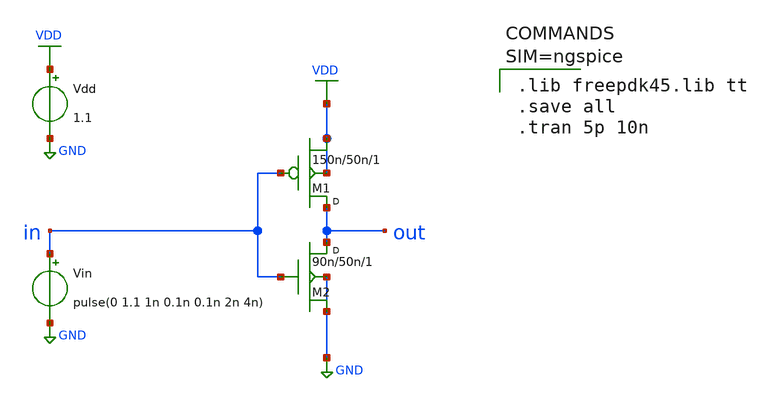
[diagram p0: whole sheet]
** sch_path: freepdk45/libs.tech/xschem/test_inverter.sch
**.subckt test_inverter
M1 out in VDD VDD pmos_vtg w=150n l=50n m=1
M2 out in GND GND nmos_vtg w=90n l=50n m=1
Vin in GND pulse(0 1.1 1n 0.1n 0.1n 2n 4n)
Vdd VDD GND 1.1
**** begin user architecture code


.lib freepdk45.lib tt
.save all
.tran 5p 10n



**** end user architecture code
**.ends
.GLOBAL VDD
.GLOBAL GND
.end
